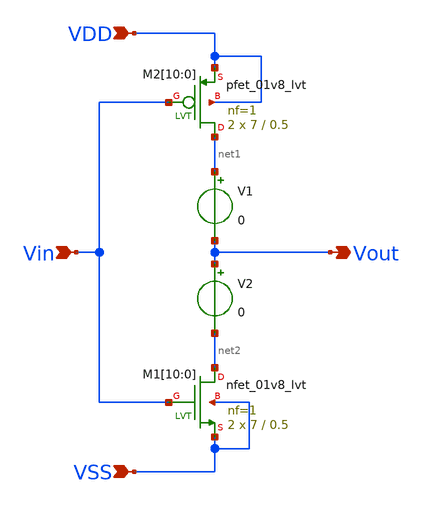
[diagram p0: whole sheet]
** sch_path: design/THESIS_EXP_RO_INVERTER_SKY130A/INV_LVT_v2.sch
**.subckt INV_LVT_v2 VDD VSS Vin Vout
*.ipin VDD
*.ipin VSS
*.ipin Vin
*.opin Vout
XM1[10] net2 Vin VSS VSS sky130_fd_pr__nfet_01v8_lvt L=0.5 W=7 nf=1 ad='int((nf+1)/2) * W/nf * 0.29'
+ as='int((nf+2)/2) * W/nf * 0.29' pd='2*int((nf+1)/2) * (W/nf + 0.29)' ps='2*int((nf+2)/2) * (W/nf + 0.29)'
+ nrd='0.29 / W' nrs='0.29 / W' sa=0 sb=0 sd=0 mult=2 m=2
XM1[9] net2 Vin VSS VSS sky130_fd_pr__nfet_01v8_lvt L=0.5 W=7 nf=1 ad='int((nf+1)/2) * W/nf * 0.29' as='int((nf+2)/2) * W/nf * 0.29'
+ pd='2*int((nf+1)/2) * (W/nf + 0.29)' ps='2*int((nf+2)/2) * (W/nf + 0.29)' nrd='0.29 / W' nrs='0.29 / W'
+ sa=0 sb=0 sd=0 mult=2 m=2
XM1[8] net2 Vin VSS VSS sky130_fd_pr__nfet_01v8_lvt L=0.5 W=7 nf=1 ad='int((nf+1)/2) * W/nf * 0.29' as='int((nf+2)/2) * W/nf * 0.29'
+ pd='2*int((nf+1)/2) * (W/nf + 0.29)' ps='2*int((nf+2)/2) * (W/nf + 0.29)' nrd='0.29 / W' nrs='0.29 / W'
+ sa=0 sb=0 sd=0 mult=2 m=2
XM1[7] net2 Vin VSS VSS sky130_fd_pr__nfet_01v8_lvt L=0.5 W=7 nf=1 ad='int((nf+1)/2) * W/nf * 0.29' as='int((nf+2)/2) * W/nf * 0.29'
+ pd='2*int((nf+1)/2) * (W/nf + 0.29)' ps='2*int((nf+2)/2) * (W/nf + 0.29)' nrd='0.29 / W' nrs='0.29 / W'
+ sa=0 sb=0 sd=0 mult=2 m=2
XM1[6] net2 Vin VSS VSS sky130_fd_pr__nfet_01v8_lvt L=0.5 W=7 nf=1 ad='int((nf+1)/2) * W/nf * 0.29' as='int((nf+2)/2) * W/nf * 0.29'
+ pd='2*int((nf+1)/2) * (W/nf + 0.29)' ps='2*int((nf+2)/2) * (W/nf + 0.29)' nrd='0.29 / W' nrs='0.29 / W'
+ sa=0 sb=0 sd=0 mult=2 m=2
XM1[5] net2 Vin VSS VSS sky130_fd_pr__nfet_01v8_lvt L=0.5 W=7 nf=1 ad='int((nf+1)/2) * W/nf * 0.29' as='int((nf+2)/2) * W/nf * 0.29'
+ pd='2*int((nf+1)/2) * (W/nf + 0.29)' ps='2*int((nf+2)/2) * (W/nf + 0.29)' nrd='0.29 / W' nrs='0.29 / W'
+ sa=0 sb=0 sd=0 mult=2 m=2
XM1[4] net2 Vin VSS VSS sky130_fd_pr__nfet_01v8_lvt L=0.5 W=7 nf=1 ad='int((nf+1)/2) * W/nf * 0.29' as='int((nf+2)/2) * W/nf * 0.29'
+ pd='2*int((nf+1)/2) * (W/nf + 0.29)' ps='2*int((nf+2)/2) * (W/nf + 0.29)' nrd='0.29 / W' nrs='0.29 / W'
+ sa=0 sb=0 sd=0 mult=2 m=2
XM1[3] net2 Vin VSS VSS sky130_fd_pr__nfet_01v8_lvt L=0.5 W=7 nf=1 ad='int((nf+1)/2) * W/nf * 0.29' as='int((nf+2)/2) * W/nf * 0.29'
+ pd='2*int((nf+1)/2) * (W/nf + 0.29)' ps='2*int((nf+2)/2) * (W/nf + 0.29)' nrd='0.29 / W' nrs='0.29 / W'
+ sa=0 sb=0 sd=0 mult=2 m=2
XM1[2] net2 Vin VSS VSS sky130_fd_pr__nfet_01v8_lvt L=0.5 W=7 nf=1 ad='int((nf+1)/2) * W/nf * 0.29' as='int((nf+2)/2) * W/nf * 0.29'
+ pd='2*int((nf+1)/2) * (W/nf + 0.29)' ps='2*int((nf+2)/2) * (W/nf + 0.29)' nrd='0.29 / W' nrs='0.29 / W'
+ sa=0 sb=0 sd=0 mult=2 m=2
XM1[1] net2 Vin VSS VSS sky130_fd_pr__nfet_01v8_lvt L=0.5 W=7 nf=1 ad='int((nf+1)/2) * W/nf * 0.29' as='int((nf+2)/2) * W/nf * 0.29'
+ pd='2*int((nf+1)/2) * (W/nf + 0.29)' ps='2*int((nf+2)/2) * (W/nf + 0.29)' nrd='0.29 / W' nrs='0.29 / W'
+ sa=0 sb=0 sd=0 mult=2 m=2
XM1[0] net2 Vin VSS VSS sky130_fd_pr__nfet_01v8_lvt L=0.5 W=7 nf=1 ad='int((nf+1)/2) * W/nf * 0.29' as='int((nf+2)/2) * W/nf * 0.29'
+ pd='2*int((nf+1)/2) * (W/nf + 0.29)' ps='2*int((nf+2)/2) * (W/nf + 0.29)' nrd='0.29 / W' nrs='0.29 / W'
+ sa=0 sb=0 sd=0 mult=2 m=2
XM2[10] net1 Vin VDD VDD sky130_fd_pr__pfet_01v8_lvt L=0.5 W=7 nf=1 ad='int((nf+1)/2) * W/nf * 0.29'
+ as='int((nf+2)/2) * W/nf * 0.29' pd='2*int((nf+1)/2) * (W/nf + 0.29)' ps='2*int((nf+2)/2) * (W/nf + 0.29)'
+ nrd='0.29 / W' nrs='0.29 / W' sa=0 sb=0 sd=0 mult=2 m=2
XM2[9] net1 Vin VDD VDD sky130_fd_pr__pfet_01v8_lvt L=0.5 W=7 nf=1 ad='int((nf+1)/2) * W/nf * 0.29' as='int((nf+2)/2) * W/nf * 0.29'
+ pd='2*int((nf+1)/2) * (W/nf + 0.29)' ps='2*int((nf+2)/2) * (W/nf + 0.29)' nrd='0.29 / W' nrs='0.29 / W'
+ sa=0 sb=0 sd=0 mult=2 m=2
XM2[8] net1 Vin VDD VDD sky130_fd_pr__pfet_01v8_lvt L=0.5 W=7 nf=1 ad='int((nf+1)/2) * W/nf * 0.29' as='int((nf+2)/2) * W/nf * 0.29'
+ pd='2*int((nf+1)/2) * (W/nf + 0.29)' ps='2*int((nf+2)/2) * (W/nf + 0.29)' nrd='0.29 / W' nrs='0.29 / W'
+ sa=0 sb=0 sd=0 mult=2 m=2
XM2[7] net1 Vin VDD VDD sky130_fd_pr__pfet_01v8_lvt L=0.5 W=7 nf=1 ad='int((nf+1)/2) * W/nf * 0.29' as='int((nf+2)/2) * W/nf * 0.29'
+ pd='2*int((nf+1)/2) * (W/nf + 0.29)' ps='2*int((nf+2)/2) * (W/nf + 0.29)' nrd='0.29 / W' nrs='0.29 / W'
+ sa=0 sb=0 sd=0 mult=2 m=2
XM2[6] net1 Vin VDD VDD sky130_fd_pr__pfet_01v8_lvt L=0.5 W=7 nf=1 ad='int((nf+1)/2) * W/nf * 0.29' as='int((nf+2)/2) * W/nf * 0.29'
+ pd='2*int((nf+1)/2) * (W/nf + 0.29)' ps='2*int((nf+2)/2) * (W/nf + 0.29)' nrd='0.29 / W' nrs='0.29 / W'
+ sa=0 sb=0 sd=0 mult=2 m=2
XM2[5] net1 Vin VDD VDD sky130_fd_pr__pfet_01v8_lvt L=0.5 W=7 nf=1 ad='int((nf+1)/2) * W/nf * 0.29' as='int((nf+2)/2) * W/nf * 0.29'
+ pd='2*int((nf+1)/2) * (W/nf + 0.29)' ps='2*int((nf+2)/2) * (W/nf + 0.29)' nrd='0.29 / W' nrs='0.29 / W'
+ sa=0 sb=0 sd=0 mult=2 m=2
XM2[4] net1 Vin VDD VDD sky130_fd_pr__pfet_01v8_lvt L=0.5 W=7 nf=1 ad='int((nf+1)/2) * W/nf * 0.29' as='int((nf+2)/2) * W/nf * 0.29'
+ pd='2*int((nf+1)/2) * (W/nf + 0.29)' ps='2*int((nf+2)/2) * (W/nf + 0.29)' nrd='0.29 / W' nrs='0.29 / W'
+ sa=0 sb=0 sd=0 mult=2 m=2
XM2[3] net1 Vin VDD VDD sky130_fd_pr__pfet_01v8_lvt L=0.5 W=7 nf=1 ad='int((nf+1)/2) * W/nf * 0.29' as='int((nf+2)/2) * W/nf * 0.29'
+ pd='2*int((nf+1)/2) * (W/nf + 0.29)' ps='2*int((nf+2)/2) * (W/nf + 0.29)' nrd='0.29 / W' nrs='0.29 / W'
+ sa=0 sb=0 sd=0 mult=2 m=2
XM2[2] net1 Vin VDD VDD sky130_fd_pr__pfet_01v8_lvt L=0.5 W=7 nf=1 ad='int((nf+1)/2) * W/nf * 0.29' as='int((nf+2)/2) * W/nf * 0.29'
+ pd='2*int((nf+1)/2) * (W/nf + 0.29)' ps='2*int((nf+2)/2) * (W/nf + 0.29)' nrd='0.29 / W' nrs='0.29 / W'
+ sa=0 sb=0 sd=0 mult=2 m=2
XM2[1] net1 Vin VDD VDD sky130_fd_pr__pfet_01v8_lvt L=0.5 W=7 nf=1 ad='int((nf+1)/2) * W/nf * 0.29' as='int((nf+2)/2) * W/nf * 0.29'
+ pd='2*int((nf+1)/2) * (W/nf + 0.29)' ps='2*int((nf+2)/2) * (W/nf + 0.29)' nrd='0.29 / W' nrs='0.29 / W'
+ sa=0 sb=0 sd=0 mult=2 m=2
XM2[0] net1 Vin VDD VDD sky130_fd_pr__pfet_01v8_lvt L=0.5 W=7 nf=1 ad='int((nf+1)/2) * W/nf * 0.29' as='int((nf+2)/2) * W/nf * 0.29'
+ pd='2*int((nf+1)/2) * (W/nf + 0.29)' ps='2*int((nf+2)/2) * (W/nf + 0.29)' nrd='0.29 / W' nrs='0.29 / W'
+ sa=0 sb=0 sd=0 mult=2 m=2
V1 net1 Vout 0
.save i(v1)
V2 Vout net2 0
.save i(v2)
**.ends
.end
